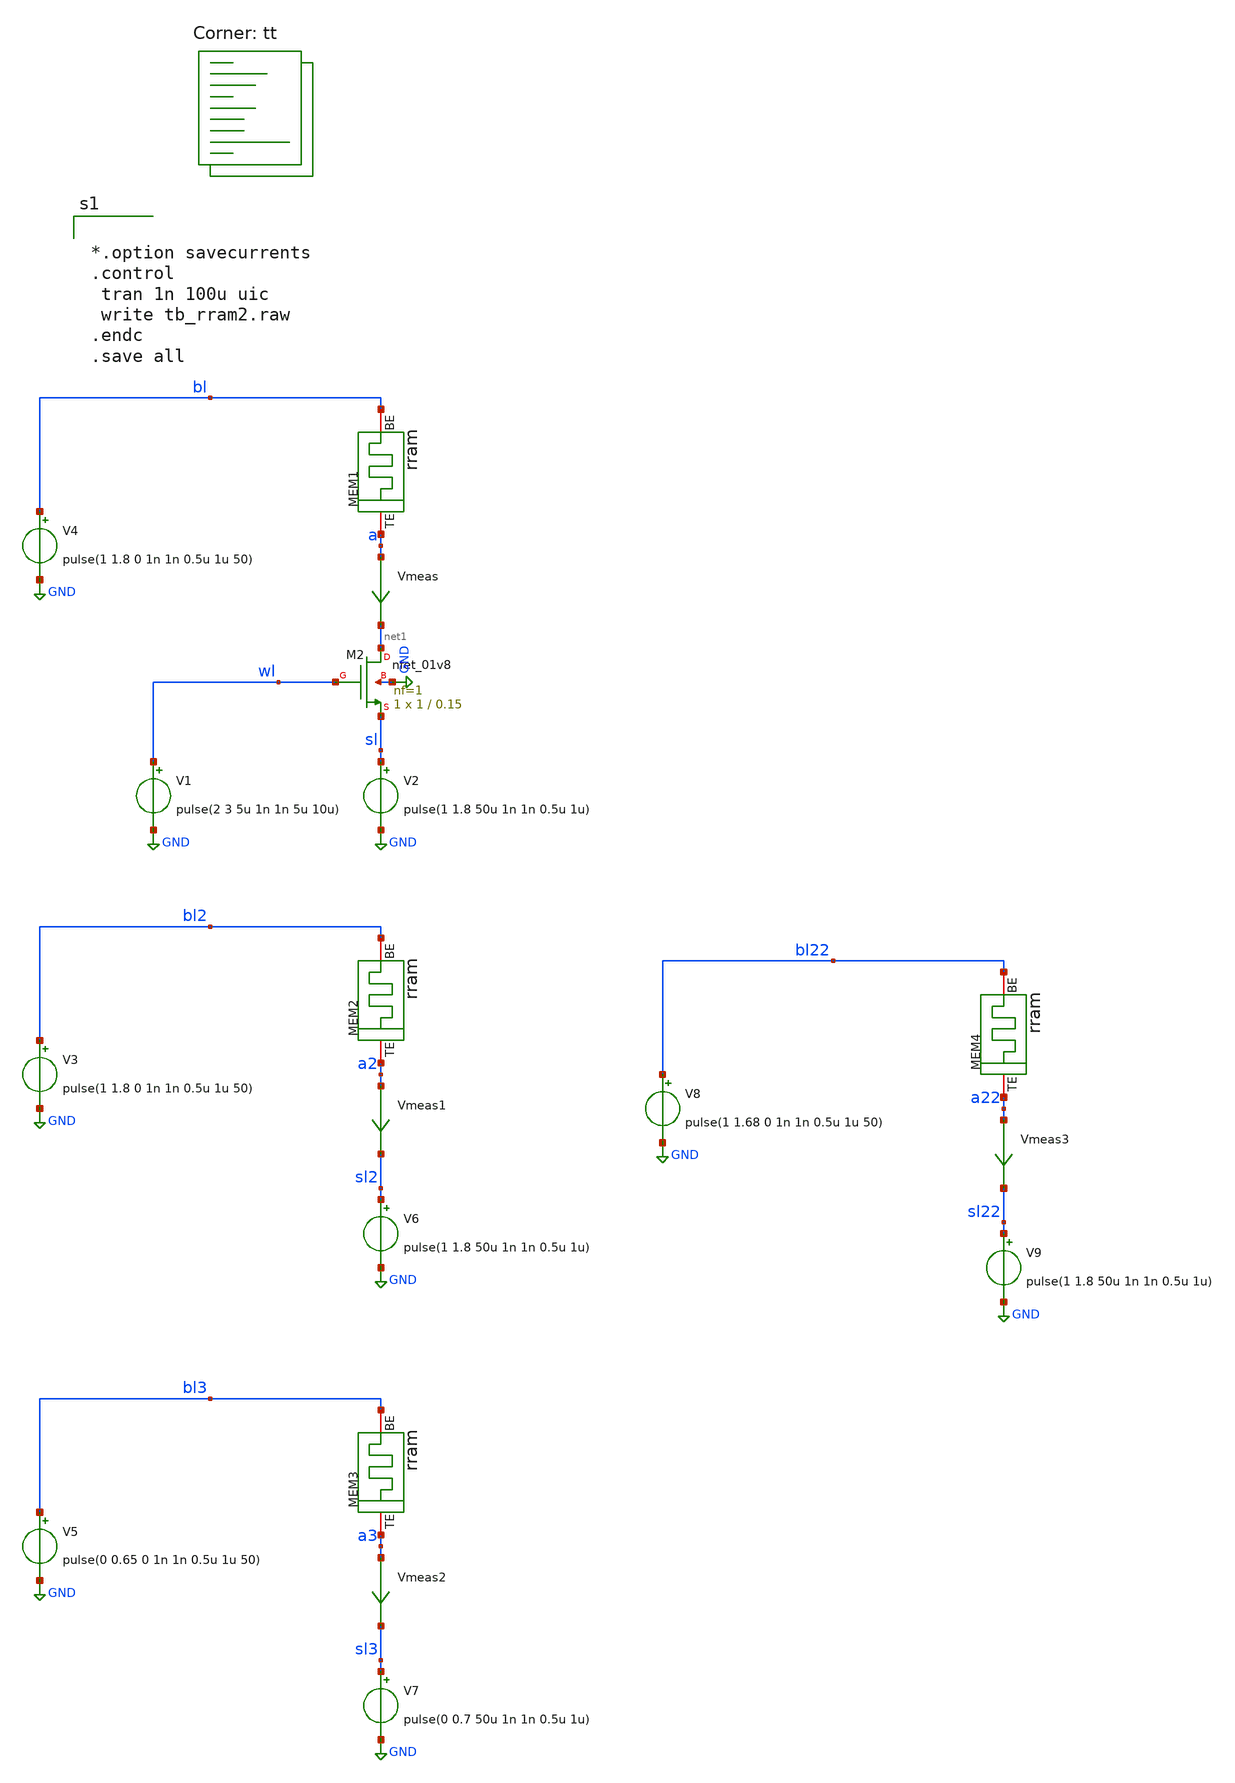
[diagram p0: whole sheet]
** sch_path: designs/tb_memristor/tb_rram2.sch
**.subckt tb_rram2
MEM1 a bl rram
V4 bl GND pulse(1 1.8 0 1n 1n 0.5u 1u 50)
XM2 net1 wl sl GND sky130_fd_pr__nfet_01v8 L=0.15 W=1 nf=1 ad='int((1 + 1)/2) * 1 / 1 * 0.29' as='int((1 + 2)/2) * 1 / 1 * 0.29'
+ pd='2*int((1 + 1)/2) * (1 / 1 + 0.29)' ps='2*int((1 + 2)/2) * (1 / 1 + 0.29)' nrd='0.29 / 1 ' nrs='0.29 / 1 '
+ sa=0 sb=0 sd=0 mult=1 m=1
V1 wl GND pulse(2 3 5u 1n 1n 5u 10u)
V2 sl GND pulse(1 1.8 50u 1n 1n 0.5u 1u)
Vmeas a net1 0
.save i(vmeas)
MEM2 a2 bl2 rram
V3 bl2 GND pulse(1 1.8 0 1n 1n 0.5u 1u 50)
V6 sl2 GND pulse(1 1.8 50u 1n 1n 0.5u 1u)
Vmeas1 a2 sl2 0
.save i(vmeas1)
MEM3 a3 bl3 rram
V5 bl3 GND pulse(0 0.65 0 1n 1n 0.5u 1u 50)
V7 sl3 GND pulse(0 0.7 50u 1n 1n 0.5u 1u)
Vmeas2 a3 sl3 0
.save i(vmeas2)
V8 bl22 GND pulse(1 1.68 0 1n 1n 0.5u 1u 50)
V9 sl22 GND pulse(1 1.8 50u 1n 1n 0.5u 1u)
Vmeas3 a22 sl22 0
.save i(vmeas3)
MEM4 a22 bl22 rram
**** begin user architecture code
.lib $::SKYWATER_MODELS/sky130.lib.spice tt


*.option savecurrents
.control
 tran 1n 100u uic
 write tb_rram2.raw
.endc
.save all

 ** opencircuitdesign pdks install
*.inc /foss/designs/spike_130/designs/memristors/rram_v0/rram.spice
.inc $PDK_ROOT/sky130A/libs.tech/ngspice/rram.spice
*.inc $::SKYWATER_MODELS/rram.spice
**** end user architecture code
**.ends
.GLOBAL GND
.end
